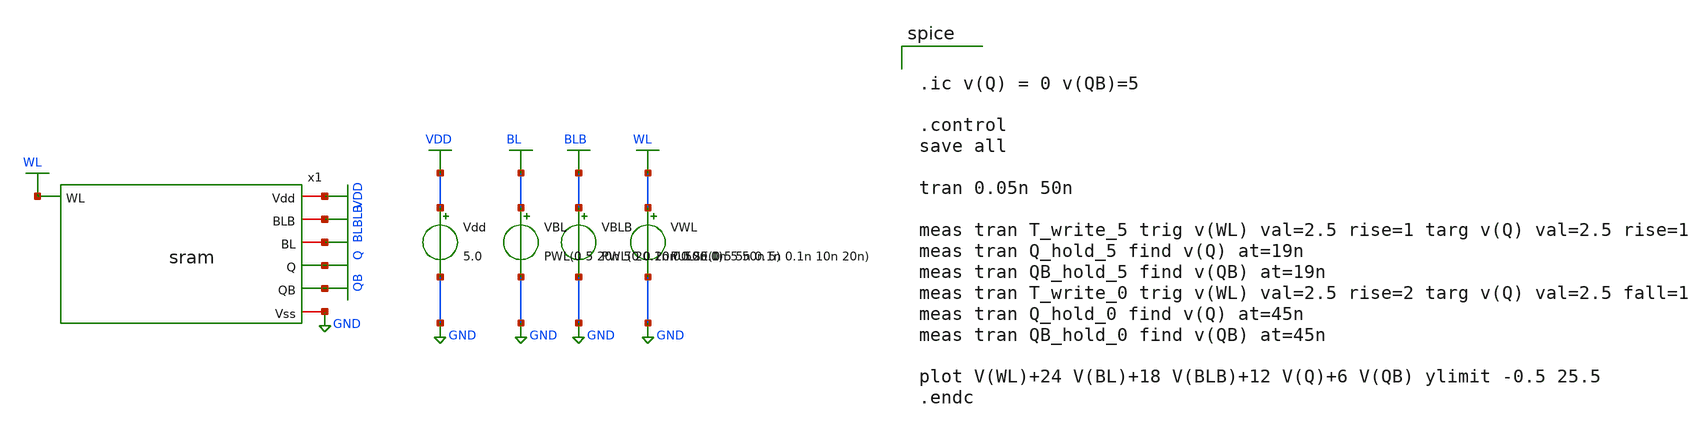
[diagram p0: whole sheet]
** sch_path: sram_tb_tran_write.sch
**.subckt sram_tb_tran_write
Vdd VDD GND 5.0
VBL BL GND PWL(0 5 20n 5 20.1n 0 50n 0)
VBLB BLB GND PWL(0 0 20n 0 20.1n 5 50n 5)
VWL WL GND PULSE(0 5 5n 0.1n 0.1n 10n 20n)
x1 WL VDD BLB BL Q QB GND sram
**** begin user architecture code
 .include $::LIB/ip62_models


.ic v(Q) = 0 v(QB)=5

.control
save all

tran 0.05n 50n

meas tran T_write_5 trig v(WL) val=2.5 rise=1 targ v(Q) val=2.5 rise=1
meas tran Q_hold_5 find v(Q) at=19n
meas tran QB_hold_5 find v(QB) at=19n
meas tran T_write_0 trig v(WL) val=2.5 rise=2 targ v(Q) val=2.5 fall=1
meas tran Q_hold_0 find v(Q) at=45n
meas tran QB_hold_0 find v(QB) at=45n

plot V(WL)+24 V(BL)+18 V(BLB)+12 V(Q)+6 V(QB) ylimit -0.5 25.5
.endc



**** end user architecture code
**.ends

* expanding   symbol:  sram.sym # of pins=7
** sym_path: sram.sym
** sch_path: sram.sch
.subckt sram WL Vdd BLB BL Q QB Vss
*.iopin Vdd
*.iopin Vss
*.iopin BLB
*.iopin BL
*.ipin WL
*.opin Q
*.opin QB
XXM1 Q QB Vss Vss NMOS w=3.4u l=1u nrd=0 nrs=0 m=1
XXM2 Q QB Vdd Vdd PMOS w=3.4u l=1u nrd=0 nrs=0 m=1
XXM3 QB Q Vss Vss NMOS w=3.4u l=1u nrd=0 nrs=0 m=1
XXM4 QB Q Vdd Vdd PMOS w=3.4u l=1u nrd=0 nrs=0 m=1
XXM7 Q WL BL Vss NMOS w=3.4u l=1u nrd=0 nrs=0 m=1
XXM6 QB WL BLB Vss NMOS w=3.4u l=1u nrd=0 nrs=0 m=1
.ends

.GLOBAL VDD
.GLOBAL GND
.GLOBAL QB
.GLOBAL Q
.GLOBAL BLB
.GLOBAL BL
.GLOBAL WL
.end
